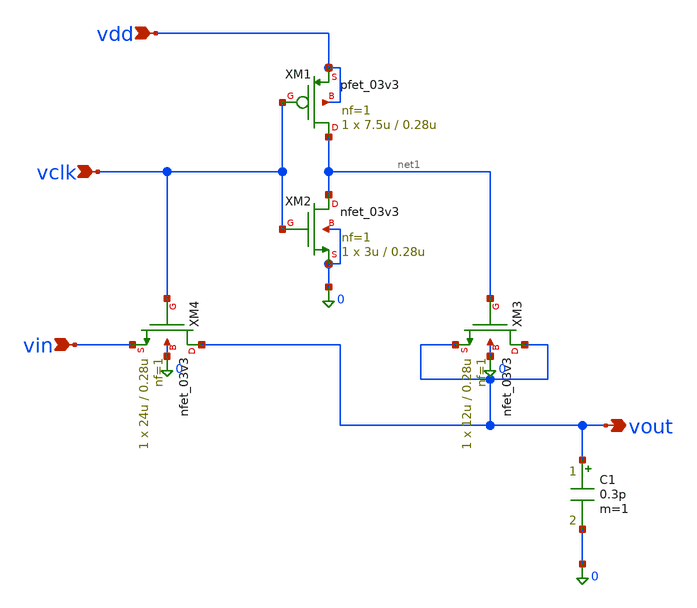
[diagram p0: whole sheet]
** sch_path: analog/blocks/transmission_gate/hold.sch
**.subckt hold vin vout vclk vdd
*.ipin vin
*.opin vout
*.ipin vclk
*.ipin vdd
XM1 net1 vclk vdd vdd pfet_03v3 L=0.28u W=7.5u nf=1 ad='int((nf+1)/2) * W/nf * 0.18u' as='int((nf+2)/2) * W/nf * 0.18u'
+ pd='2*int((nf+1)/2) * (W/nf + 0.18u)' ps='2*int((nf+2)/2) * (W/nf + 0.18u)' nrd='0.18u / W' nrs='0.18u / W'
+ sa=0 sb=0 sd=0 m=1
XM2 net1 vclk 0 0 nfet_03v3 L=0.28u W=3u nf=1 ad='int((nf+1)/2) * W/nf * 0.18u' as='int((nf+2)/2) * W/nf * 0.18u'
+ pd='2*int((nf+1)/2) * (W/nf + 0.18u)' ps='2*int((nf+2)/2) * (W/nf + 0.18u)' nrd='0.18u / W' nrs='0.18u / W'
+ sa=0 sb=0 sd=0 m=1
XM3 vout net1 vout 0 nfet_03v3 L=0.28u W=12u nf=1 ad='int((nf+1)/2) * W/nf * 0.18u' as='int((nf+2)/2) * W/nf * 0.18u'
+ pd='2*int((nf+1)/2) * (W/nf + 0.18u)' ps='2*int((nf+2)/2) * (W/nf + 0.18u)' nrd='0.18u / W' nrs='0.18u / W'
+ sa=0 sb=0 sd=0 m=1
XM4 vout vclk vin 0 nfet_03v3 L=0.28u W=24u nf=1 ad='int((nf+1)/2) * W/nf * 0.18u' as='int((nf+2)/2) * W/nf * 0.18u'
+ pd='2*int((nf+1)/2) * (W/nf + 0.18u)' ps='2*int((nf+2)/2) * (W/nf + 0.18u)' nrd='0.18u / W' nrs='0.18u / W'
+ sa=0 sb=0 sd=0 m=1
C1 vout 0 0.3p m=1
**.ends
.end
